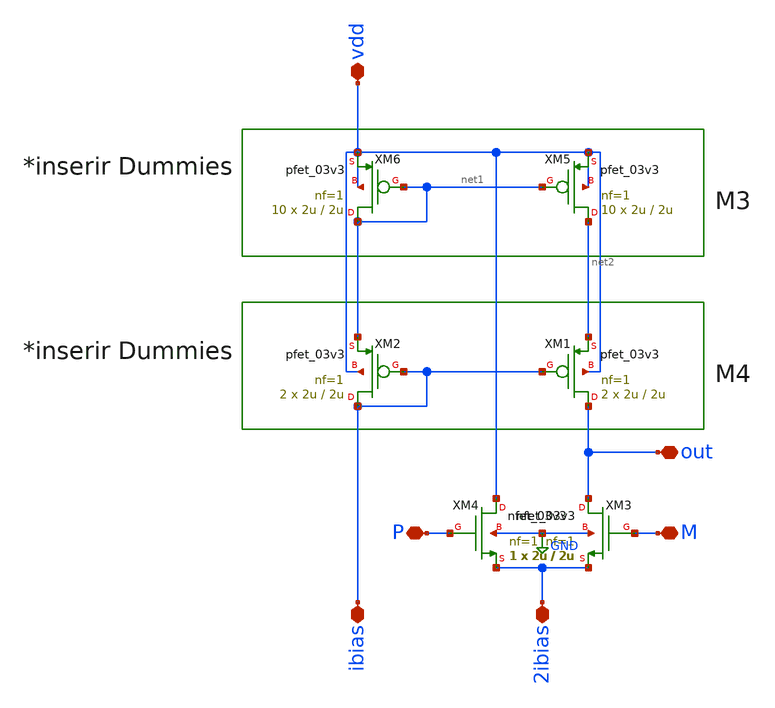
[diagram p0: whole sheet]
** sch_path: Clock_Reference/symbols_clock/VCIS.sch
**.subckt VCIS 2ibias ibias P M out vdd
*.iopin 2ibias
*.iopin ibias
*.iopin P
*.iopin M
*.iopin out
*.iopin vdd
XM1 out ibias net2 vdd pfet_03v3 L=2u W=2u nf=1 ad='int((nf+1)/2) * W/nf * 0.18u' as='int((nf+2)/2) * W/nf * 0.18u'
+ pd='2*int((nf+1)/2) * (W/nf + 0.18u)' ps='2*int((nf+2)/2) * (W/nf + 0.18u)' nrd='0.18u / W' nrs='0.18u / W'
+ sa=0 sb=0 sd=0 m=2
XM2 ibias ibias net1 vdd pfet_03v3 L=2u W=2u nf=1 ad='int((nf+1)/2) * W/nf * 0.18u' as='int((nf+2)/2) * W/nf * 0.18u'
+ pd='2*int((nf+1)/2) * (W/nf + 0.18u)' ps='2*int((nf+2)/2) * (W/nf + 0.18u)' nrd='0.18u / W' nrs='0.18u / W'
+ sa=0 sb=0 sd=0 m=2
XM3 out M 2ibias GND nfet_03v3 L=2u W=2u nf=1 ad='int((nf+1)/2) * W/nf * 0.18u' as='int((nf+2)/2) * W/nf * 0.18u'
+ pd='2*int((nf+1)/2) * (W/nf + 0.18u)' ps='2*int((nf+2)/2) * (W/nf + 0.18u)' nrd='0.18u / W' nrs='0.18u / W'
+ sa=0 sb=0 sd=0 m=1
XM4 vdd P 2ibias GND nfet_03v3 L=2u W=2u nf=1 ad='int((nf+1)/2) * W/nf * 0.18u' as='int((nf+2)/2) * W/nf * 0.18u'
+ pd='2*int((nf+1)/2) * (W/nf + 0.18u)' ps='2*int((nf+2)/2) * (W/nf + 0.18u)' nrd='0.18u / W' nrs='0.18u / W'
+ sa=0 sb=0 sd=0 m=1
XM5 net2 net1 vdd vdd pfet_03v3 L=2u W=2u nf=1 ad='int((nf+1)/2) * W/nf * 0.18u' as='int((nf+2)/2) * W/nf * 0.18u'
+ pd='2*int((nf+1)/2) * (W/nf + 0.18u)' ps='2*int((nf+2)/2) * (W/nf + 0.18u)' nrd='0.18u / W' nrs='0.18u / W'
+ sa=0 sb=0 sd=0 m=10
XM6 net1 net1 vdd vdd pfet_03v3 L=2u W=2u nf=1 ad='int((nf+1)/2) * W/nf * 0.18u' as='int((nf+2)/2) * W/nf * 0.18u'
+ pd='2*int((nf+1)/2) * (W/nf + 0.18u)' ps='2*int((nf+2)/2) * (W/nf + 0.18u)' nrd='0.18u / W' nrs='0.18u / W'
+ sa=0 sb=0 sd=0 m=10
**.ends
.GLOBAL GND
.end
